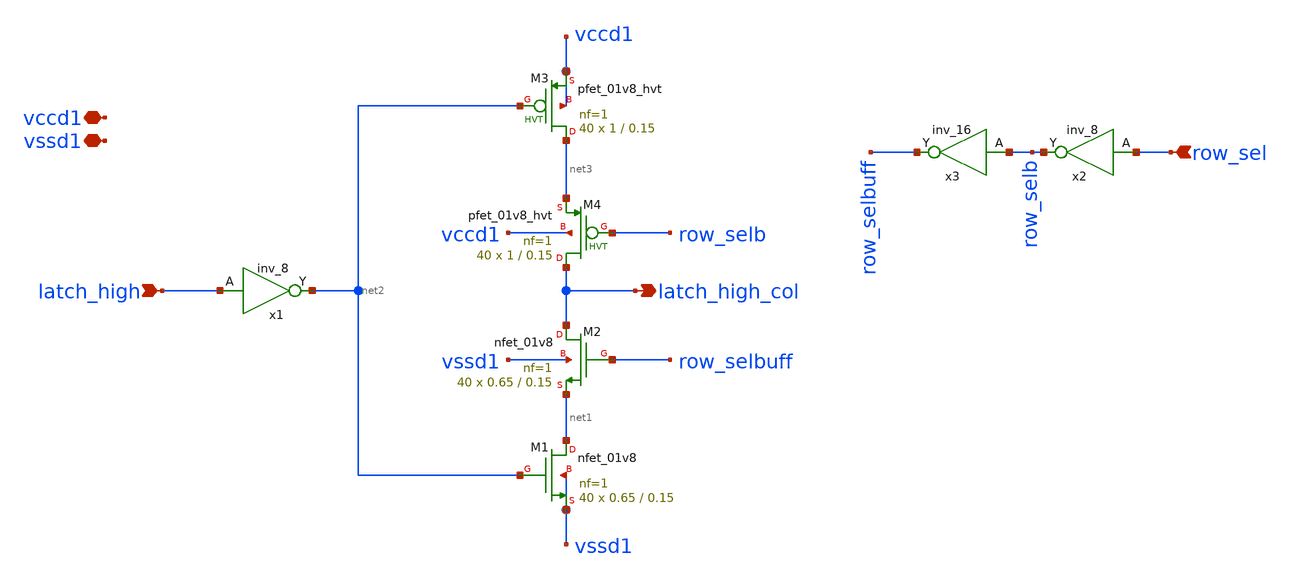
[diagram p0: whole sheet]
** sch_path: xschem/comp_out_sel.sch
**.subckt comp_out_sel vccd1 vssd1 latch_high row_sel latch_high_col
*.iopin vccd1
*.iopin vssd1
*.ipin latch_high
*.ipin row_sel
*.opin latch_high_col
x1 latch_high vssd1 vssd1 vccd1 vccd1 net2 sky130_fd_sc_hd__inv_8
XM1 net1 net2 vssd1 vssd1 sky130_fd_pr__nfet_01v8 L=0.15 W=0.65 nf=1 ad='int((nf+1)/2) * W/nf * 0.29'
+ as='int((nf+2)/2) * W/nf * 0.29' pd='2*int((nf+1)/2) * (W/nf + 0.29)' ps='2*int((nf+2)/2) * (W/nf + 0.29)'
+ nrd='0.29 / W' nrs='0.29 / W' sa=0 sb=0 sd=0 mult=40 m=40
XM2 latch_high_col row_selbuff net1 vssd1 sky130_fd_pr__nfet_01v8 L=0.15 W=0.65 nf=1 ad='int((nf+1)/2) * W/nf * 0.29'
+ as='int((nf+2)/2) * W/nf * 0.29' pd='2*int((nf+1)/2) * (W/nf + 0.29)' ps='2*int((nf+2)/2) * (W/nf + 0.29)'
+ nrd='0.29 / W' nrs='0.29 / W' sa=0 sb=0 sd=0 mult=40 m=40
XM3 net3 net2 vccd1 vccd1 sky130_fd_pr__pfet_01v8_hvt L=0.15 W=1 nf=1 ad='int((nf+1)/2) * W/nf * 0.29'
+ as='int((nf+2)/2) * W/nf * 0.29' pd='2*int((nf+1)/2) * (W/nf + 0.29)' ps='2*int((nf+2)/2) * (W/nf + 0.29)'
+ nrd='0.29 / W' nrs='0.29 / W' sa=0 sb=0 sd=0 mult=40 m=40
XM4 latch_high_col row_selb net3 vccd1 sky130_fd_pr__pfet_01v8_hvt L=0.15 W=1 nf=1 ad='int((nf+1)/2) * W/nf * 0.29'
+ as='int((nf+2)/2) * W/nf * 0.29' pd='2*int((nf+1)/2) * (W/nf + 0.29)' ps='2*int((nf+2)/2) * (W/nf + 0.29)'
+ nrd='0.29 / W' nrs='0.29 / W' sa=0 sb=0 sd=0 mult=40 m=40
x2 row_sel vssd1 vssd1 vccd1 vccd1 row_selb sky130_fd_sc_hd__inv_8
x3 row_selb vssd1 vssd1 vccd1 vccd1 row_selbuff sky130_fd_sc_hd__inv_16
**** begin user architecture code
 .lib $::SKYWATER_MODELS/sky130.lib.spice tt
.include $::SKYWATER_STDCELLS/sky130_fd_sc_hd.spice

**** end user architecture code
**.ends
.end
